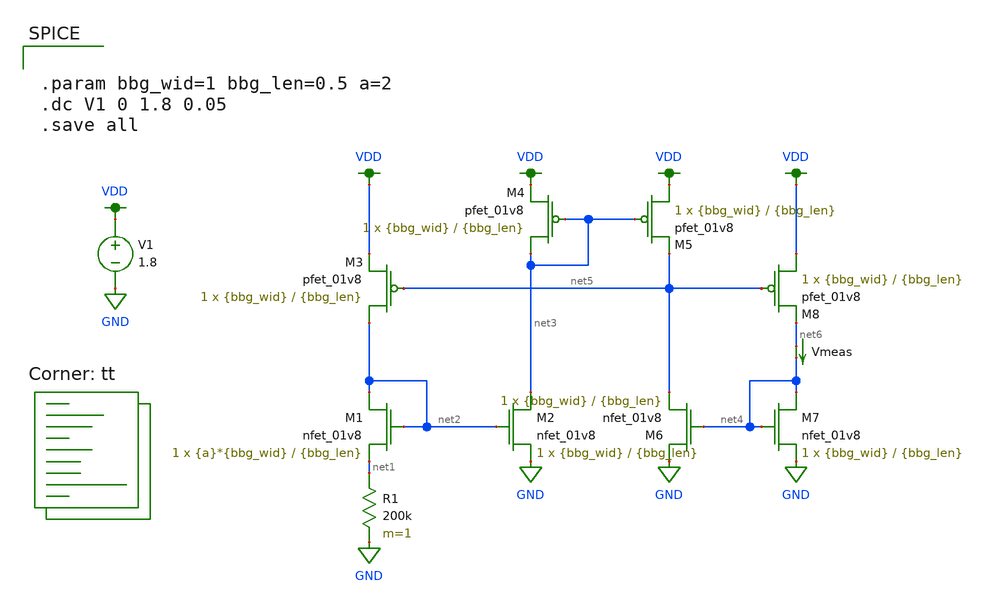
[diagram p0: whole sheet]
** sch_path: bbg.sch
**.subckt bbg
XM1 net2 net2 net1 GND sky130_fd_pr__nfet_01v8 L={bbg_len} W={a}*{bbg_wid} nf=1 ad='int((nf+1)/2) * W/nf * 0.29'
+ as='int((nf+2)/2) * W/nf * 0.29' pd='2*int((nf+1)/2) * (W/nf + 0.29)' ps='2*int((nf+2)/2) * (W/nf + 0.29)'
+ nrd='0.29 / W' nrs='0.29 / W' sa=0 sb=0 sd=0 mult=1 m=1
XM2 net3 net2 GND GND sky130_fd_pr__nfet_01v8 L={bbg_len} W={bbg_wid} nf=1 ad='int((nf+1)/2) * W/nf * 0.29'
+ as='int((nf+2)/2) * W/nf * 0.29' pd='2*int((nf+1)/2) * (W/nf + 0.29)' ps='2*int((nf+2)/2) * (W/nf + 0.29)'
+ nrd='0.29 / W' nrs='0.29 / W' sa=0 sb=0 sd=0 mult=1 m=1
R1 net1 GND 200k m=1
XM3 net2 net5 VDD VDD sky130_fd_pr__pfet_01v8 L={bbg_len} W={bbg_wid} nf=1 ad='int((nf+1)/2) * W/nf * 0.29'
+ as='int((nf+2)/2) * W/nf * 0.29' pd='2*int((nf+1)/2) * (W/nf + 0.29)' ps='2*int((nf+2)/2) * (W/nf + 0.29)'
+ nrd='0.29 / W' nrs='0.29 / W' sa=0 sb=0 sd=0 mult=1 m=1
V1 VDD GND 1.8
Vmeas net6 net4 0
.save i(vmeas)
XM6 GND net4 net5 GND sky130_fd_pr__nfet_01v8 L={bbg_len} W={bbg_wid} nf=1 ad='int((nf+1)/2) * W/nf * 0.29'
+ as='int((nf+2)/2) * W/nf * 0.29' pd='2*int((nf+1)/2) * (W/nf + 0.29)' ps='2*int((nf+2)/2) * (W/nf + 0.29)'
+ nrd='0.29 / W' nrs='0.29 / W' sa=0 sb=0 sd=0 mult=1 m=1
XM7 net4 net4 GND GND sky130_fd_pr__nfet_01v8 L={bbg_len} W={bbg_wid} nf=1 ad='int((nf+1)/2) * W/nf * 0.29'
+ as='int((nf+2)/2) * W/nf * 0.29' pd='2*int((nf+1)/2) * (W/nf + 0.29)' ps='2*int((nf+2)/2) * (W/nf + 0.29)'
+ nrd='0.29 / W' nrs='0.29 / W' sa=0 sb=0 sd=0 mult=1 m=1
XM4 net3 net3 VDD VDD sky130_fd_pr__pfet_01v8 L={bbg_len} W={bbg_wid} nf=1 ad='int((nf+1)/2) * W/nf * 0.29'
+ as='int((nf+2)/2) * W/nf * 0.29' pd='2*int((nf+1)/2) * (W/nf + 0.29)' ps='2*int((nf+2)/2) * (W/nf + 0.29)'
+ nrd='0.29 / W' nrs='0.29 / W' sa=0 sb=0 sd=0 mult=1 m=1
XM5 VDD net3 net5 VDD sky130_fd_pr__pfet_01v8 L={bbg_len} W={bbg_wid} nf=1 ad='int((nf+1)/2) * W/nf * 0.29'
+ as='int((nf+2)/2) * W/nf * 0.29' pd='2*int((nf+1)/2) * (W/nf + 0.29)' ps='2*int((nf+2)/2) * (W/nf + 0.29)'
+ nrd='0.29 / W' nrs='0.29 / W' sa=0 sb=0 sd=0 mult=1 m=1
XM8 VDD net5 net6 VDD sky130_fd_pr__pfet_01v8 L={bbg_len} W={bbg_wid} nf=1 ad='int((nf+1)/2) * W/nf * 0.29'
+ as='int((nf+2)/2) * W/nf * 0.29' pd='2*int((nf+1)/2) * (W/nf + 0.29)' ps='2*int((nf+2)/2) * (W/nf + 0.29)'
+ nrd='0.29 / W' nrs='0.29 / W' sa=0 sb=0 sd=0 mult=1 m=1
**** begin user architecture code


.param bbg_wid=1 bbg_len=0.5 a=2
.dc V1 0 1.8 0.05
.save all

.lib $::SKYWATER_MODELS/sky130.lib.spice tt
**** end user architecture code
**.ends
.GLOBAL GND
.GLOBAL VDD
.end
